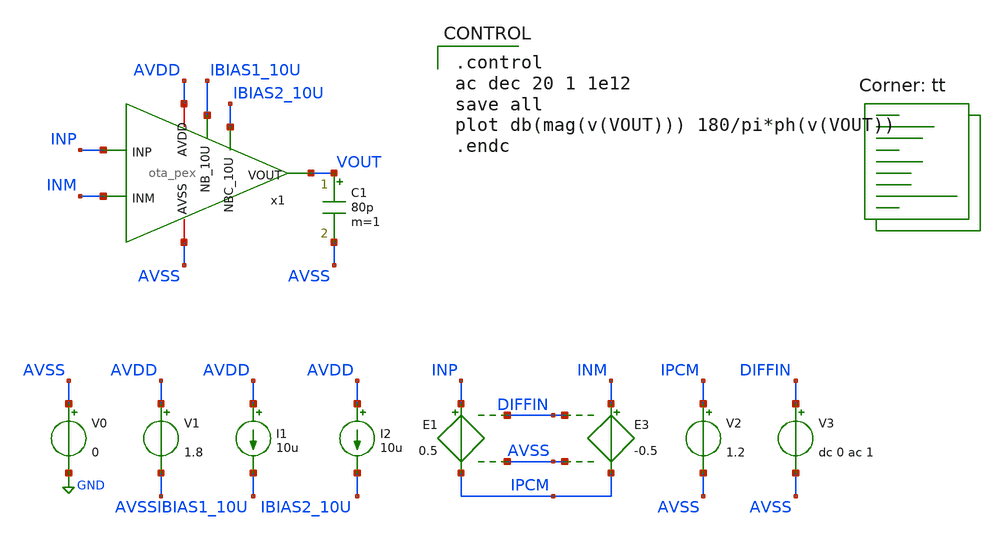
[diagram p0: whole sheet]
** sch_path: ISSCC25/submitted_notebooks/analog_vibes/sim_pex/xschem/tb_ac_pex.sch
**.subckt tb_ac_pex
V0 AVSS GND 0
V1 AVDD AVSS 1.8
I1 AVDD IBIAS1_10U 10u
I2 AVDD IBIAS2_10U 10u
E1 INP IPCM DIFFIN AVSS 0.5
E3 INM IPCM DIFFIN AVSS -0.5
V2 IPCM AVSS 1.2
V3 DIFFIN AVSS dc 0 ac 1
C1 VOUT AVSS 80p m=1
x1 AVDD AVSS INP INM IBIAS1_10U IBIAS2_10U VOUT ota_pex
**** begin user architecture code
.lib $::SKYWATER_MODELS/sky130.lib.spice tt

.control
ac dec 20 1 1e12
save all
plot db(mag(v(VOUT))) 180/pi*ph(v(VOUT))
.endc

**** end user architecture code
**.ends

* expanding   symbol:  ota_pex.sym # of pins=7
** sym_path: ISSCC25/submitted_notebooks/analog_vibes/sim_pex/xschem/ota_pex.sym
.include /home/sscspico/test_tools/coc_analog_vibes/ISSCC25/submitted_notebooks/analog_vibes/sim_pex/xschem/ota_pex.spice
.GLOBAL GND
.end
